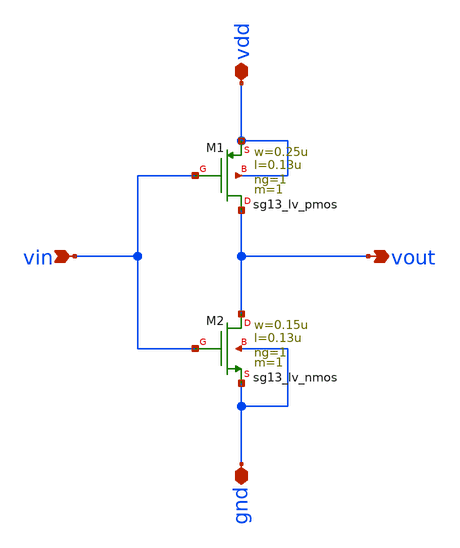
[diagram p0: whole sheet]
** sch_path: design/schematics/inverter.sch
**.subckt inverter vdd gnd vin vout
*.iopin vdd
*.iopin gnd
*.ipin vin
*.opin vout
XM2 vout vin gnd gnd sg13_lv_nmos w=0.15u l=0.13u ng=1 m=1 mm_ok=1
XM1 vout vin vdd vdd sg13_lv_pmos w=0.25u l=0.13u ng=1 m=1 mm_ok=1
**.ends
.end
